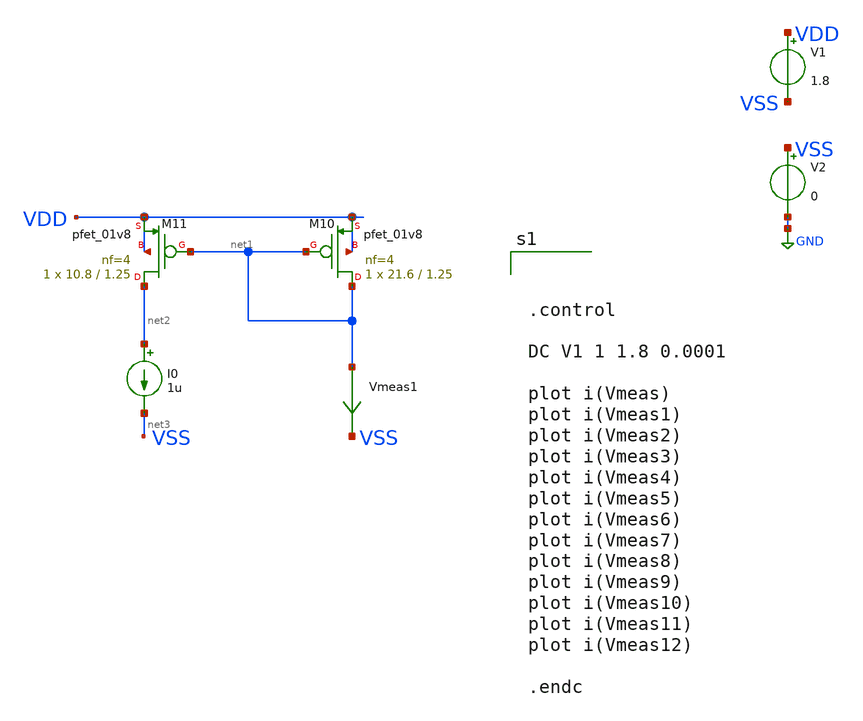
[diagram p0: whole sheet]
** sch_path: bandgap-final/bias-net/bias-net.sch
**.subckt bias-net
V1 net4 VSS 1.8
V2 net5 GND 0
XM10 net1 net1 VDD VDD sky130_fd_pr__pfet_01v8 L=1.25 W=21.6 nf=4 ad='int((nf+1)/2) * W/nf * 0.29' as='int((nf+2)/2) * W/nf * 0.29'
+ pd='2*int((nf+1)/2) * (W/nf + 0.29)' ps='2*int((nf+2)/2) * (W/nf + 0.29)' nrd='0.29 / W' nrs='0.29 / W'
+ sa=0 sb=0 sd=0 mult=1 m=1
XM11 net2 net1 VDD VDD sky130_fd_pr__pfet_01v8 L=1.25 W=10.8 nf=4 ad='int((nf+1)/2) * W/nf * 0.29' as='int((nf+2)/2) * W/nf * 0.29'
+ pd='2*int((nf+1)/2) * (W/nf + 0.29)' ps='2*int((nf+2)/2) * (W/nf + 0.29)' nrd='0.29 / W' nrs='0.29 / W'
+ sa=0 sb=0 sd=0 mult=1 m=1
Vmeas1 net1 net6 0
.save i(vmeas1)
I0 net2 net3 1u
**** begin user architecture code



.control

DC V1 1 1.8 0.0001

plot i(Vmeas)
plot i(Vmeas1)
plot i(Vmeas2)
plot i(Vmeas3)
plot i(Vmeas4)
plot i(Vmeas5)
plot i(Vmeas6)
plot i(Vmeas7)
plot i(Vmeas8)
plot i(Vmeas9)
plot i(Vmeas10)
plot i(Vmeas11)
plot i(Vmeas12)

.endc






** opencircuitdesign pdks install
.lib $::SKYWATER_MODELS/sky130.lib.spice tt


**** end user architecture code
**.ends
.GLOBAL GND
.end
